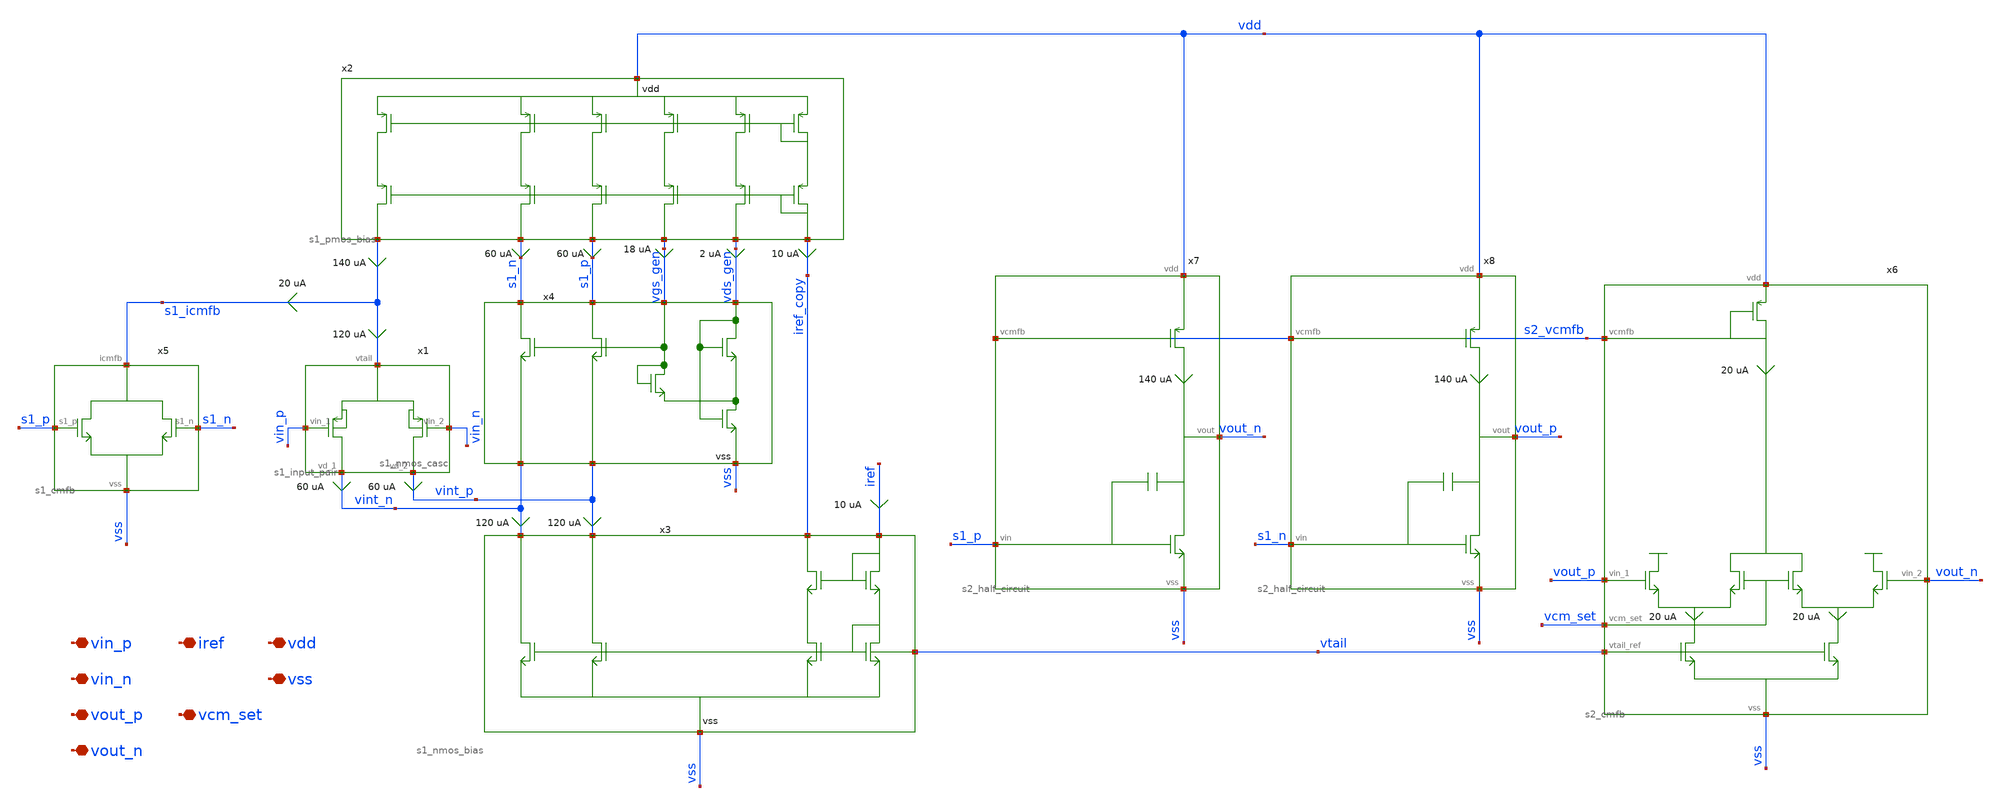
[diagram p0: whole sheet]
** sch_path: xschem/archive/ota/ota.sch
**.subckt ota vin_p vin_n vout_p vout_n iref vdd vss vcm_set
*.iopin vin_p
*.iopin vin_n
*.iopin vout_p
*.iopin vout_n
*.iopin iref
*.iopin vdd
*.iopin vss
*.iopin vcm_set
x1 vint_n vint_p vin_p vin_n s1_icmfb s1_input_pair
x2 vdd s1_icmfb s1_n s1_p vgs_gen vds_gen iref_copy s1_pmos_bias
x3 iref iref_copy vint_n vint_p vss vtail s1_nmos_bias
x4 s1_n s1_p vint_n vint_p vgs_gen vds_gen vss s1_nmos_casc
x5 s1_icmfb s1_p s1_n vss s1_cmfb
x6 vout_p vout_n vcm_set vtail s2_vcmfb vdd vss s2_cmfb
x7 s2_vcmfb vdd vss s1_p vout_n s2_half_circuit
x8 s2_vcmfb vdd vss s1_n vout_p s2_half_circuit
**.ends
.end
